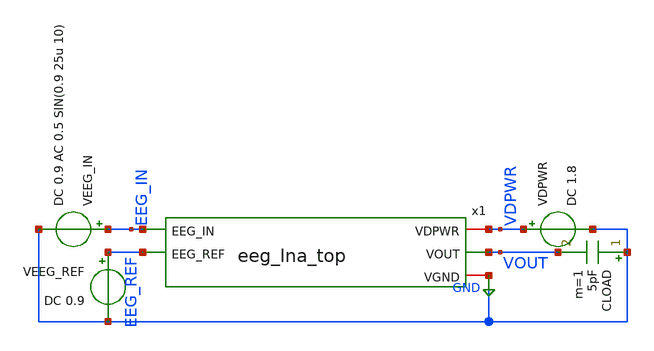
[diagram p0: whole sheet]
** sch_path: xschem/tb_eeg_lna_top.sch
**.subckt tb_eeg_lna_top
x1 EEG_IN VDPWR VOUT GND EEG_REF eeg_lna_top
VDPWR VDPWR GND DC 1.8
VEEG_REF EEG_REF GND DC 0.9
VEEG_IN EEG_IN GND DC 0.9 AC 0.5 SIN(0.9 25u 10)
CLOAD GND VOUT 5pF m=1
**** begin user architecture code


.lib /foss/pdks/sky130A/libs.tech/ngspice/sky130.lib.spice tt_mm

.ic v(VOUT)=0.5 v(x1.ota_inp)=0.5 v(x1.ota_inn)=0.5    v(x1.x_ota.tail_p)=1.5 v(x1.x_ota.EEG_IN)=0.5
+    v(x1.x_rpseudo_p.EEG_IN)=0.5 v(x1.x_rpseudo_fb.EEG_IN)=0.5

.nodeset v(VOUT)=0.5 v(x1.ota_inp)=0.5 v(x1.ota_inn)=0.5         v(x1.x_ota.tail_p)=1.5
+ v(x1.x_ota.EEG_IN)=0.5         v(x1.x_rpseudo_p.EEG_IN)=0.5 v(x1.x_rpseudo_fb.EEG_IN)=0.5

.option savecurrents
.option rshunt=1e15
.option gmin=1e-15
.option method=gear
.option cshunt=1e-15

.control
op
echo ===== Bias Verification =====
print @m.x1.x_ota.xmtail[id]
print v(x1.x_ota.tail_p)
print v(x1.bias_p)
print @m.x1.x_ota.xmdiff_p[id]
print @m.x1.x_ota.xmdiff_n[id]

echo ===== Operating Point =====
print v(x1.ota_inp)
print v(x1.ota_inn)
print v(x1.ota_inp)-v(x1.ota_inn)
print v(VOUT)

echo ===== Transient =====
tran 1m 20
plot v(EEG_IN)
plot v(x1.ota_inp)
plot v(x1.ota_inn)
plot v(x1.ota_inp)-v(x1.ota_inn)
plot v(VOUT)
plot v(VOUT)-0.84

echo ===== Noise =====
noise v(VOUT) veeg_in dec 100 0.5 100

* Active plot is the totals plot — print integrated values
print inoise_total
print onoise_total

* Switch to the spectrum plot to see vs frequency
setplot previous
plot db(inoise_spectrum)
plot db(onoise_spectrum)

echo ===== AC =====
ac dec 100 0.01 100k
plot db(v(VOUT)/v(EEG_IN))

plot db(v(x1.ota_inp)/v(EEG_IN))
plot db(v(x1.ota_inn)/v(EEG_REF))
plot db(v(VOUT)/(v(x1.ota_inp)-v(x1.ota_inn)))

.endc


**** end user architecture code
**.ends

* expanding   symbol:  eeg_lna_top.sym # of pins=5
** sym_path: xschem/eeg_lna_top.sym
** sch_path: xschem/eeg_lna_top.sch
.subckt eeg_lna_top EEG_IN VDPWR VOUT VGND EEG_REF
*.ipin EEG_IN
*.ipin EEG_REF
*.iopin VDPWR
*.iopin VGND
*.opin VOUT
x2 net3 net4 pseudo_res
x1 net5 net6 pseudo_res
XCACP EEG_IN net2 sky130_fd_pr__cap_mim_m3_1 W=1 L=1 MF=1 m=1
XC_REF EEG_REF net1 sky130_fd_pr__cap_mim_m3_1 W=1 L=1 MF=1 m=1
x3 net7 net8 net2 net1 net9 net10 ota_5t
.ends


* expanding   symbol:  pseudo_res.sym # of pins=2
** sym_path: xschem/pseudo_res.sym
** sch_path: xschem/pseudo_res.sch
.subckt pseudo_res B A
*.iopin A
*.iopin B
XM1_PSEUDO_RES B B A A sky130_fd_pr__pfet_01v8 L=10 W=0.42 nf=1 ad='int((1 + 1)/2) * 0.42 / 1 * 0.29'
+ as='int((1 + 2)/2) * 0.42 / 1 * 0.29' pd='2*int((1 + 1)/2) * (0.42 / 1 + 0.29)' ps='2*int((1 + 2)/2) * (0.42 / 1 + 0.29)'
+ nrd='0.29 / 0.42 ' nrs='0.29 / 0.42 ' sa=0 sb=0 sd=0 mult=1 m=1
XM2_PSEUDO_RES A A B B sky130_fd_pr__pfet_01v8 L=10 W=0.42 nf=1 ad='int((1 + 1)/2) * 0.42 / 1 * 0.29'
+ as='int((1 + 2)/2) * 0.42 / 1 * 0.29' pd='2*int((1 + 1)/2) * (0.42 / 1 + 0.29)' ps='2*int((1 + 2)/2) * (0.42 / 1 + 0.29)'
+ nrd='0.29 / 0.42 ' nrs='0.29 / 0.42 ' sa=0 sb=0 sd=0 mult=1 m=1
.ends


* expanding   symbol:  ota_5t.sym # of pins=6
** sym_path: xschem-new/ota_5t.sym
** sch_path: xschem-new/ota_5t.sch
.subckt ota_5t BIAS_P VDPWR VIN_P VIN_N VOUT VGND
*.ipin VIN_P
*.ipin VIN_N
*.ipin BIAS_P
*.iopin VDPWR
*.iopin VGND
*.opin VOUT
XMDIFF_P net1 VIN_P TAIL_P VDPWR sky130_fd_pr__pfet_01v8 L=4 W=48 nf=1 ad='int((1 + 1)/2) * 48 / 1 * 0.29'
+ as='int((1 + 2)/2) * 48 / 1 * 0.29' pd='2*int((1 + 1)/2) * (48 / 1 + 0.29)' ps='2*int((1 + 2)/2) * (48 / 1 + 0.29)'
+ nrd='0.29 / 48 ' nrs='0.29 / 48 ' sa=0 sb=0 sd=0 mult=1 m=1
XMDIFF_N VOUT VIN_N TAIL_P VDPWR sky130_fd_pr__pfet_01v8 L=4 W=48 nf=1 ad='int((1 + 1)/2) * 48 / 1 * 0.29'
+ as='int((1 + 2)/2) * 48 / 1 * 0.29' pd='2*int((1 + 1)/2) * (48 / 1 + 0.29)' ps='2*int((1 + 2)/2) * (48 / 1 + 0.29)'
+ nrd='0.29 / 48 ' nrs='0.29 / 48 ' sa=0 sb=0 sd=0 mult=1 m=1
XMTAIL TAIL_P BIAS_P VDPWR VDPWR sky130_fd_pr__pfet_01v8 L=8 W=0.5 nf=1 ad='int((1 + 1)/2) * 0.5 / 1 * 0.29'
+ as='int((1 + 2)/2) * 0.5 / 1 * 0.29' pd='2*int((1 + 1)/2) * (0.5 / 1 + 0.29)' ps='2*int((1 + 2)/2) * (0.5 / 1 + 0.29)'
+ nrd='0.29 / 0.5 ' nrs='0.29 / 0.5 ' sa=0 sb=0 sd=0 mult=1 m=1
XMLOAD_REF net1 net1 VGND VGND sky130_fd_pr__nfet_01v8 L=16 W=8 nf=1 ad='int((1 + 1)/2) * 8 / 1 * 0.29'
+ as='int((1 + 2)/2) * 8 / 1 * 0.29' pd='2*int((1 + 1)/2) * (8 / 1 + 0.29)' ps='2*int((1 + 2)/2) * (8 / 1 + 0.29)'
+ nrd='0.29 / 8 ' nrs='0.29 / 8 ' sa=0 sb=0 sd=0 mult=1 m=1
XMLOAD_OUT VOUT net1 VGND VGND sky130_fd_pr__nfet_01v8 L=16 W=8 nf=1 ad='int((1 + 1)/2) * 8 / 1 * 0.29'
+ as='int((1 + 2)/2) * 8 / 1 * 0.29' pd='2*int((1 + 1)/2) * (8 / 1 + 0.29)' ps='2*int((1 + 2)/2) * (8 / 1 + 0.29)'
+ nrd='0.29 / 8 ' nrs='0.29 / 8 ' sa=0 sb=0 sd=0 mult=1 m=1
.ends

.GLOBAL GND
.end
